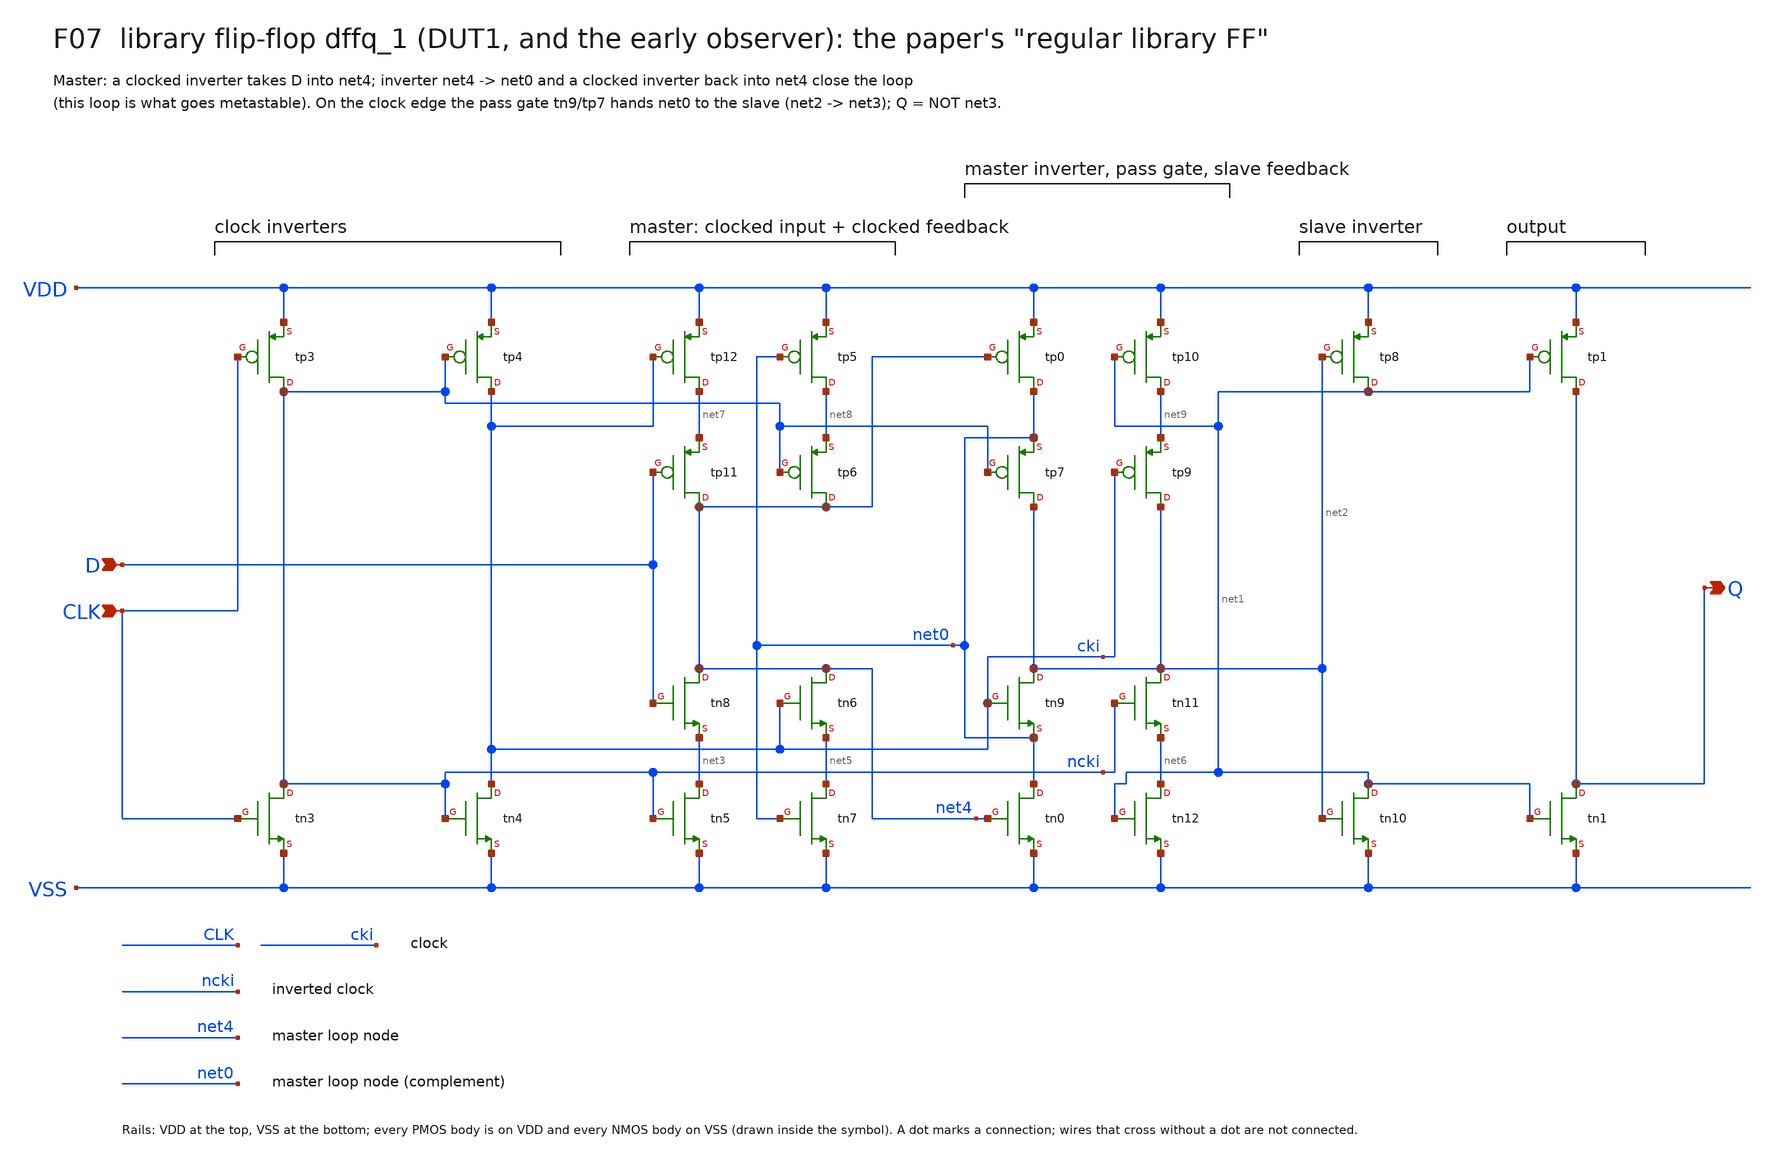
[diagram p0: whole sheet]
** sch_path: xschem/focus/F07_library_flipflop.sch
**.subckt F07_library_flipflop D CLK Q
*.ipin D
*.ipin CLK
*.opin Q
Xtn3 ncki CLK VSS VSS nfet_05v0 L=0.6u W=0.405u nf=1 m=1
Xtn4 cki ncki VSS VSS nfet_05v0 L=0.6u W=0.405u nf=1 m=1
Xtn5 net3 ncki VSS VSS nfet_05v0 L=0.6u W=0.36u nf=1 m=1
Xtn8 net4 D net3 VSS nfet_05v0 L=0.6u W=0.36u nf=1 m=1
Xtn6 net4 cki net5 VSS nfet_05v0 L=0.6u W=0.36u nf=1 m=1
Xtn7 net5 net0 VSS VSS nfet_05v0 L=0.6u W=0.36u nf=1 m=1
Xtn0 net0 net4 VSS VSS nfet_05v0 L=0.6u W=0.36u nf=1 m=1
Xtn9 net2 cki net0 VSS nfet_05v0 L=0.6u W=0.36u nf=1 m=1
Xtn11 net2 ncki net6 VSS nfet_05v0 L=0.6u W=0.36u nf=1 m=1
Xtn12 net6 net1 VSS VSS nfet_05v0 L=0.6u W=0.36u nf=1 m=1
Xtn10 net1 net2 VSS VSS nfet_05v0 L=0.6u W=0.4u nf=1 m=1
Xtn1 Q net1 VSS VSS nfet_05v0 L=0.6u W=0.82u nf=1 m=1
Xtp3 ncki CLK VDD VDD pfet_05v0 L=0.5u W=0.865u nf=1 m=1
Xtp4 cki ncki VDD VDD pfet_05v0 L=0.5u W=0.865u nf=1 m=1
Xtp12 net7 cki VDD VDD pfet_05v0 L=0.5u W=0.36u nf=1 m=1
Xtp11 net4 D net7 VDD pfet_05v0 L=0.5u W=0.36u nf=1 m=1
Xtp6 net4 ncki net8 VDD pfet_05v0 L=0.5u W=0.36u nf=1 m=1
Xtp5 net8 net0 VDD VDD pfet_05v0 L=0.5u W=0.36u nf=1 m=1
Xtp0 net0 net4 VDD VDD pfet_05v0 L=0.5u W=0.36u nf=1 m=1
Xtp7 net2 ncki net0 VDD pfet_05v0 L=0.5u W=0.36u nf=1 m=1
Xtp9 net2 cki net9 VDD pfet_05v0 L=0.5u W=0.36u nf=1 m=1
Xtp10 net9 net1 VDD VDD pfet_05v0 L=0.5u W=0.36u nf=1 m=1
Xtp8 net1 net2 VDD VDD pfet_05v0 L=0.5u W=0.8u nf=1 m=1
Xtp1 Q net1 VDD VDD pfet_05v0 L=0.5u W=1.22u nf=1 m=1
**.ends
.end
